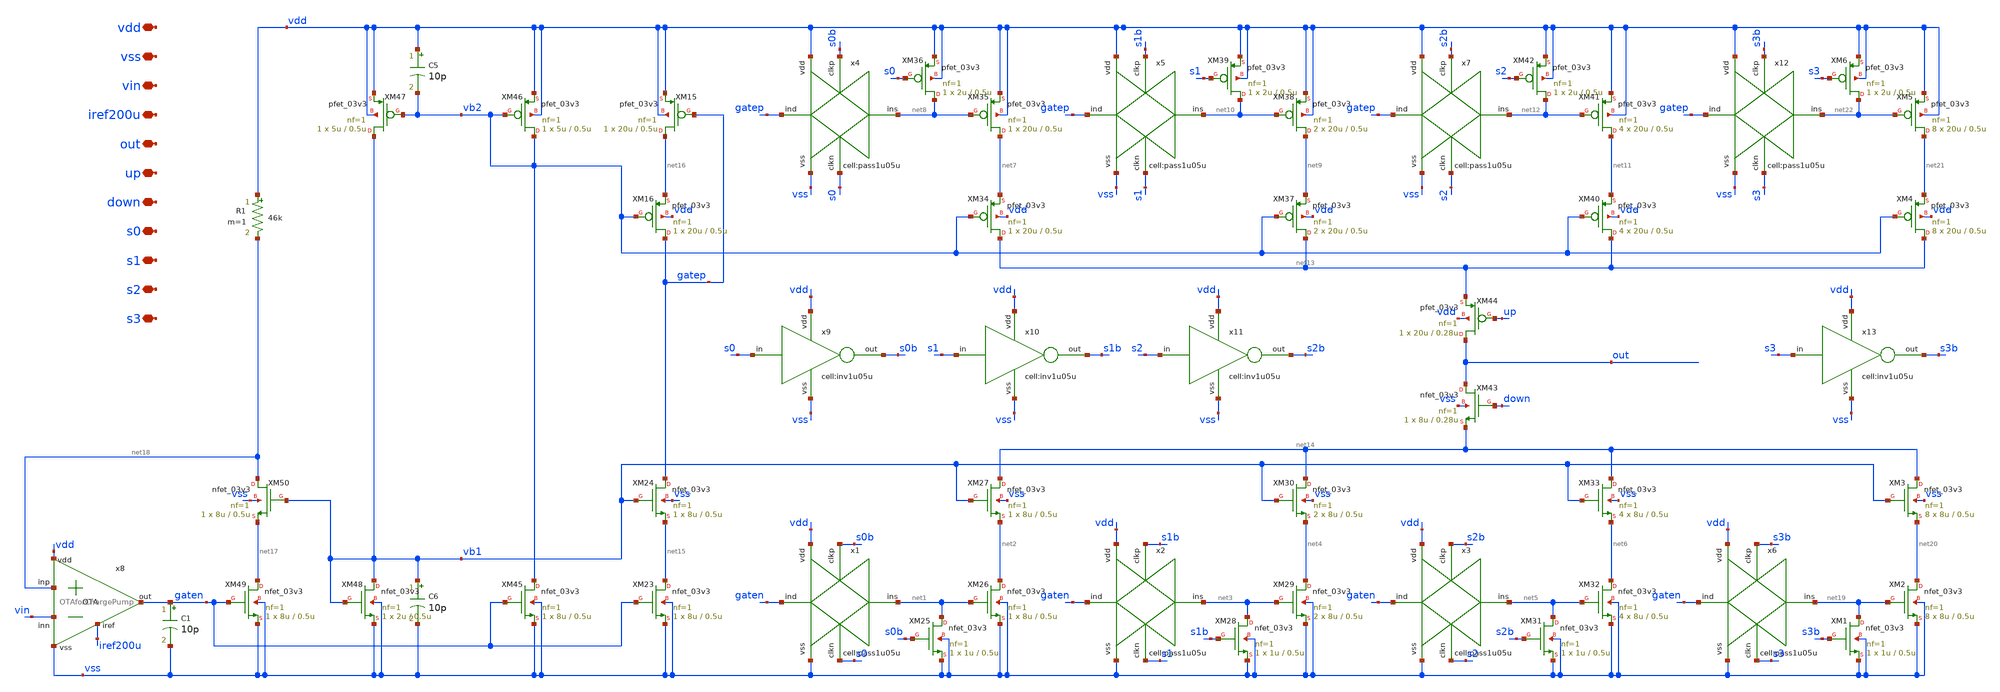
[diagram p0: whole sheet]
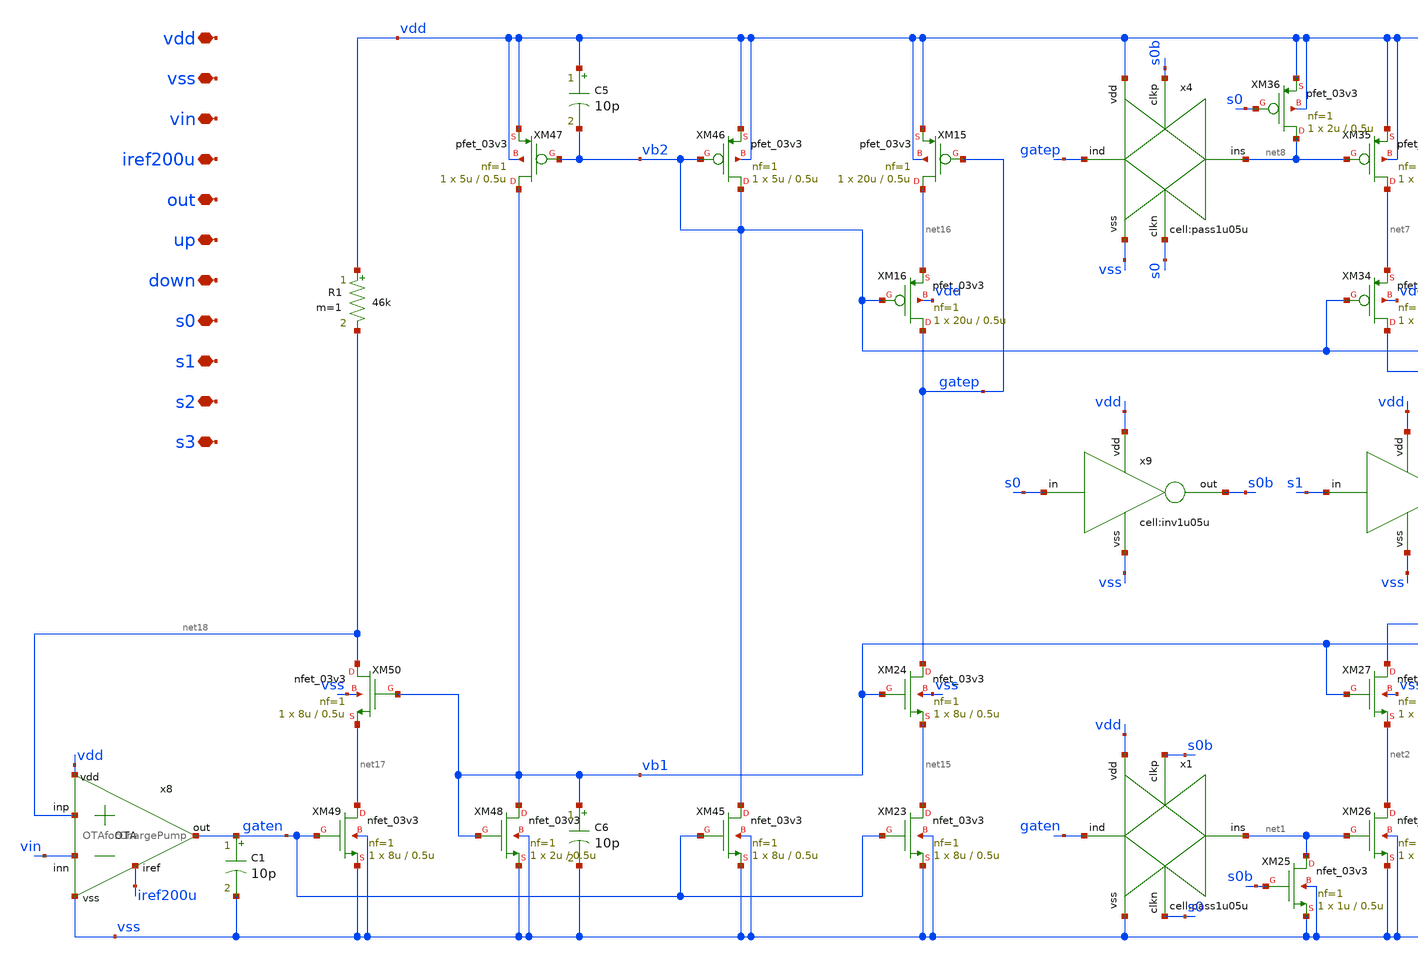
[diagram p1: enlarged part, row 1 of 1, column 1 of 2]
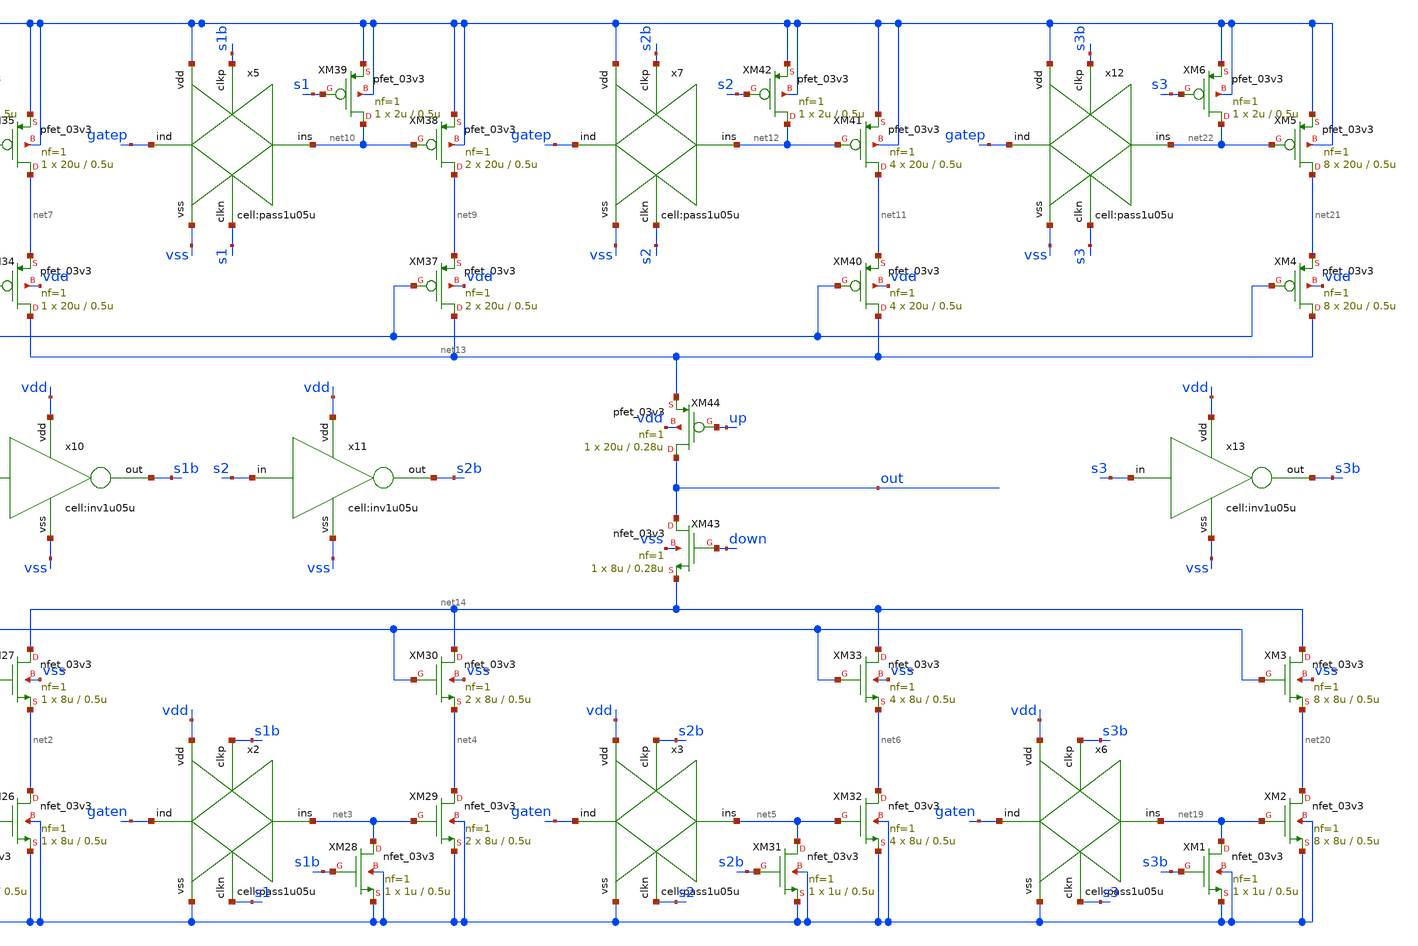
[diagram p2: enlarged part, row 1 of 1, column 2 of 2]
** sch_path: designs/libs/qw_core_analog/PCP1248X/PCP1248X.sch
**.subckt PCP1248X vdd vss vin iref200u out up down s0 s1 s2 s3
*.iopin vdd
*.iopin vss
*.iopin vin
*.iopin iref200u
*.iopin out
*.iopin up
*.iopin down
*.iopin s0
*.iopin s1
*.iopin s2
*.iopin s3
x1 gaten vss s0 net1 s0b vdd pass1u05u
XM25 net1 s0b vss vss nfet_03v3 L=0.5u W=1u nf=1 ad='int((nf+1)/2) * W/nf * 0.18u' as='int((nf+2)/2) * W/nf * 0.18u'
+ pd='2*int((nf+1)/2) * (W/nf + 0.18u)' ps='2*int((nf+2)/2) * (W/nf + 0.18u)' nrd='0.18u / W' nrs='0.18u / W'
+ sa=0 sb=0 sd=0 m=1
XM26 net2 net1 vss vss nfet_03v3 L=0.5u W=8u nf=1 ad='int((nf+1)/2) * W/nf * 0.18u' as='int((nf+2)/2) * W/nf * 0.18u'
+ pd='2*int((nf+1)/2) * (W/nf + 0.18u)' ps='2*int((nf+2)/2) * (W/nf + 0.18u)' nrd='0.18u / W' nrs='0.18u / W'
+ sa=0 sb=0 sd=0 m=1
XM27 net14 vb1 net2 vss nfet_03v3 L=0.5u W=8u nf=1 ad='int((nf+1)/2) * W/nf * 0.18u' as='int((nf+2)/2) * W/nf * 0.18u'
+ pd='2*int((nf+1)/2) * (W/nf + 0.18u)' ps='2*int((nf+2)/2) * (W/nf + 0.18u)' nrd='0.18u / W' nrs='0.18u / W'
+ sa=0 sb=0 sd=0 m=1
x2 gaten vss s1 net3 s1b vdd pass1u05u
XM28 net3 s1b vss vss nfet_03v3 L=0.5u W=1u nf=1 ad='int((nf+1)/2) * W/nf * 0.18u' as='int((nf+2)/2) * W/nf * 0.18u'
+ pd='2*int((nf+1)/2) * (W/nf + 0.18u)' ps='2*int((nf+2)/2) * (W/nf + 0.18u)' nrd='0.18u / W' nrs='0.18u / W'
+ sa=0 sb=0 sd=0 m=1
XM29 net4 net3 vss vss nfet_03v3 L=0.5u W=8u nf=1 ad='int((nf+1)/2) * W/nf * 0.18u' as='int((nf+2)/2) * W/nf * 0.18u'
+ pd='2*int((nf+1)/2) * (W/nf + 0.18u)' ps='2*int((nf+2)/2) * (W/nf + 0.18u)' nrd='0.18u / W' nrs='0.18u / W'
+ sa=0 sb=0 sd=0 m=2
XM30 net14 vb1 net4 vss nfet_03v3 L=0.5u W=8u nf=1 ad='int((nf+1)/2) * W/nf * 0.18u' as='int((nf+2)/2) * W/nf * 0.18u'
+ pd='2*int((nf+1)/2) * (W/nf + 0.18u)' ps='2*int((nf+2)/2) * (W/nf + 0.18u)' nrd='0.18u / W' nrs='0.18u / W'
+ sa=0 sb=0 sd=0 m=2
x3 gaten vss s2 net5 s2b vdd pass1u05u
XM31 net5 s2b vss vss nfet_03v3 L=0.5u W=1u nf=1 ad='int((nf+1)/2) * W/nf * 0.18u' as='int((nf+2)/2) * W/nf * 0.18u'
+ pd='2*int((nf+1)/2) * (W/nf + 0.18u)' ps='2*int((nf+2)/2) * (W/nf + 0.18u)' nrd='0.18u / W' nrs='0.18u / W'
+ sa=0 sb=0 sd=0 m=1
XM32 net6 net5 vss vss nfet_03v3 L=0.5u W=8u nf=1 ad='int((nf+1)/2) * W/nf * 0.18u' as='int((nf+2)/2) * W/nf * 0.18u'
+ pd='2*int((nf+1)/2) * (W/nf + 0.18u)' ps='2*int((nf+2)/2) * (W/nf + 0.18u)' nrd='0.18u / W' nrs='0.18u / W'
+ sa=0 sb=0 sd=0 m=4
XM33 net14 vb1 net6 vss nfet_03v3 L=0.5u W=8u nf=1 ad='int((nf+1)/2) * W/nf * 0.18u' as='int((nf+2)/2) * W/nf * 0.18u'
+ pd='2*int((nf+1)/2) * (W/nf + 0.18u)' ps='2*int((nf+2)/2) * (W/nf + 0.18u)' nrd='0.18u / W' nrs='0.18u / W'
+ sa=0 sb=0 sd=0 m=4
XM34 net13 vb2 net7 vdd pfet_03v3 L=0.5u W=20u nf=1 ad='int((nf+1)/2) * W/nf * 0.18u' as='int((nf+2)/2) * W/nf * 0.18u'
+ pd='2*int((nf+1)/2) * (W/nf + 0.18u)' ps='2*int((nf+2)/2) * (W/nf + 0.18u)' nrd='0.18u / W' nrs='0.18u / W'
+ sa=0 sb=0 sd=0 m=1
XM35 net7 net8 vdd vdd pfet_03v3 L=0.5u W=20u nf=1 ad='int((nf+1)/2) * W/nf * 0.18u' as='int((nf+2)/2) * W/nf * 0.18u'
+ pd='2*int((nf+1)/2) * (W/nf + 0.18u)' ps='2*int((nf+2)/2) * (W/nf + 0.18u)' nrd='0.18u / W' nrs='0.18u / W'
+ sa=0 sb=0 sd=0 m=1
x4 gatep vss s0 net8 s0b vdd pass1u05u
XM36 net8 s0 vdd vdd pfet_03v3 L=0.5u W=2u nf=1 ad='int((nf+1)/2) * W/nf * 0.18u' as='int((nf+2)/2) * W/nf * 0.18u'
+ pd='2*int((nf+1)/2) * (W/nf + 0.18u)' ps='2*int((nf+2)/2) * (W/nf + 0.18u)' nrd='0.18u / W' nrs='0.18u / W'
+ sa=0 sb=0 sd=0 m=1
XM37 net13 vb2 net9 vdd pfet_03v3 L=0.5u W=20u nf=1 ad='int((nf+1)/2) * W/nf * 0.18u' as='int((nf+2)/2) * W/nf * 0.18u'
+ pd='2*int((nf+1)/2) * (W/nf + 0.18u)' ps='2*int((nf+2)/2) * (W/nf + 0.18u)' nrd='0.18u / W' nrs='0.18u / W'
+ sa=0 sb=0 sd=0 m=2
XM38 net9 net10 vdd vdd pfet_03v3 L=0.5u W=20u nf=1 ad='int((nf+1)/2) * W/nf * 0.18u' as='int((nf+2)/2) * W/nf * 0.18u'
+ pd='2*int((nf+1)/2) * (W/nf + 0.18u)' ps='2*int((nf+2)/2) * (W/nf + 0.18u)' nrd='0.18u / W' nrs='0.18u / W'
+ sa=0 sb=0 sd=0 m=2
x5 gatep vss s1 net10 s1b vdd pass1u05u
XM39 net10 s1 vdd vdd pfet_03v3 L=0.5u W=2u nf=1 ad='int((nf+1)/2) * W/nf * 0.18u' as='int((nf+2)/2) * W/nf * 0.18u'
+ pd='2*int((nf+1)/2) * (W/nf + 0.18u)' ps='2*int((nf+2)/2) * (W/nf + 0.18u)' nrd='0.18u / W' nrs='0.18u / W'
+ sa=0 sb=0 sd=0 m=1
XM40 net13 vb2 net11 vdd pfet_03v3 L=0.5u W=20u nf=1 ad='int((nf+1)/2) * W/nf * 0.18u' as='int((nf+2)/2) * W/nf * 0.18u'
+ pd='2*int((nf+1)/2) * (W/nf + 0.18u)' ps='2*int((nf+2)/2) * (W/nf + 0.18u)' nrd='0.18u / W' nrs='0.18u / W'
+ sa=0 sb=0 sd=0 m=4
XM41 net11 net12 vdd vdd pfet_03v3 L=0.5u W=20u nf=1 ad='int((nf+1)/2) * W/nf * 0.18u' as='int((nf+2)/2) * W/nf * 0.18u'
+ pd='2*int((nf+1)/2) * (W/nf + 0.18u)' ps='2*int((nf+2)/2) * (W/nf + 0.18u)' nrd='0.18u / W' nrs='0.18u / W'
+ sa=0 sb=0 sd=0 m=4
x7 gatep vss s2 net12 s2b vdd pass1u05u
XM42 net12 s2 vdd vdd pfet_03v3 L=0.5u W=2u nf=1 ad='int((nf+1)/2) * W/nf * 0.18u' as='int((nf+2)/2) * W/nf * 0.18u'
+ pd='2*int((nf+1)/2) * (W/nf + 0.18u)' ps='2*int((nf+2)/2) * (W/nf + 0.18u)' nrd='0.18u / W' nrs='0.18u / W'
+ sa=0 sb=0 sd=0 m=1
XM43 out down net14 vss nfet_03v3 L=0.28u W=8u nf=1 ad='int((nf+1)/2) * W/nf * 0.18u' as='int((nf+2)/2) * W/nf * 0.18u'
+ pd='2*int((nf+1)/2) * (W/nf + 0.18u)' ps='2*int((nf+2)/2) * (W/nf + 0.18u)' nrd='0.18u / W' nrs='0.18u / W'
+ sa=0 sb=0 sd=0 m=1
XM44 out up net13 vdd pfet_03v3 L=0.28u W=20u nf=1 ad='int((nf+1)/2) * W/nf * 0.18u' as='int((nf+2)/2) * W/nf * 0.18u'
+ pd='2*int((nf+1)/2) * (W/nf + 0.18u)' ps='2*int((nf+2)/2) * (W/nf + 0.18u)' nrd='0.18u / W' nrs='0.18u / W'
+ sa=0 sb=0 sd=0 m=1
XM15 net16 gatep vdd vdd pfet_03v3 L=0.5u W=20u nf=1 ad='int((nf+1)/2) * W/nf * 0.18u' as='int((nf+2)/2) * W/nf * 0.18u'
+ pd='2*int((nf+1)/2) * (W/nf + 0.18u)' ps='2*int((nf+2)/2) * (W/nf + 0.18u)' nrd='0.18u / W' nrs='0.18u / W'
+ sa=0 sb=0 sd=0 m=1
XM16 gatep vb2 net16 vdd pfet_03v3 L=0.5u W=20u nf=1 ad='int((nf+1)/2) * W/nf * 0.18u' as='int((nf+2)/2) * W/nf * 0.18u'
+ pd='2*int((nf+1)/2) * (W/nf + 0.18u)' ps='2*int((nf+2)/2) * (W/nf + 0.18u)' nrd='0.18u / W' nrs='0.18u / W'
+ sa=0 sb=0 sd=0 m=1
XM23 net15 gaten vss vss nfet_03v3 L=0.5u W=8u nf=1 ad='int((nf+1)/2) * W/nf * 0.18u' as='int((nf+2)/2) * W/nf * 0.18u'
+ pd='2*int((nf+1)/2) * (W/nf + 0.18u)' ps='2*int((nf+2)/2) * (W/nf + 0.18u)' nrd='0.18u / W' nrs='0.18u / W'
+ sa=0 sb=0 sd=0 m=1
XM24 gatep vb1 net15 vss nfet_03v3 L=0.5u W=8u nf=1 ad='int((nf+1)/2) * W/nf * 0.18u' as='int((nf+2)/2) * W/nf * 0.18u'
+ pd='2*int((nf+1)/2) * (W/nf + 0.18u)' ps='2*int((nf+2)/2) * (W/nf + 0.18u)' nrd='0.18u / W' nrs='0.18u / W'
+ sa=0 sb=0 sd=0 m=1
XM45 vb2 gaten vss vss nfet_03v3 L=0.5u W=8u nf=1 ad='int((nf+1)/2) * W/nf * 0.18u' as='int((nf+2)/2) * W/nf * 0.18u'
+ pd='2*int((nf+1)/2) * (W/nf + 0.18u)' ps='2*int((nf+2)/2) * (W/nf + 0.18u)' nrd='0.18u / W' nrs='0.18u / W'
+ sa=0 sb=0 sd=0 m=1
XM46 vb2 vb2 vdd vdd pfet_03v3 L=0.5u W=5u nf=1 ad='int((nf+1)/2) * W/nf * 0.18u' as='int((nf+2)/2) * W/nf * 0.18u'
+ pd='2*int((nf+1)/2) * (W/nf + 0.18u)' ps='2*int((nf+2)/2) * (W/nf + 0.18u)' nrd='0.18u / W' nrs='0.18u / W'
+ sa=0 sb=0 sd=0 m=1
XM47 vb1 vb2 vdd vdd pfet_03v3 L=0.5u W=5u nf=1 ad='int((nf+1)/2) * W/nf * 0.18u' as='int((nf+2)/2) * W/nf * 0.18u'
+ pd='2*int((nf+1)/2) * (W/nf + 0.18u)' ps='2*int((nf+2)/2) * (W/nf + 0.18u)' nrd='0.18u / W' nrs='0.18u / W'
+ sa=0 sb=0 sd=0 m=1
XM48 vb1 vb1 vss vss nfet_03v3 L=0.5u W=2u nf=1 ad='int((nf+1)/2) * W/nf * 0.18u' as='int((nf+2)/2) * W/nf * 0.18u'
+ pd='2*int((nf+1)/2) * (W/nf + 0.18u)' ps='2*int((nf+2)/2) * (W/nf + 0.18u)' nrd='0.18u / W' nrs='0.18u / W'
+ sa=0 sb=0 sd=0 m=1
XM49 net17 gaten vss vss nfet_03v3 L=0.5u W=8u nf=1 ad='int((nf+1)/2) * W/nf * 0.18u' as='int((nf+2)/2) * W/nf * 0.18u'
+ pd='2*int((nf+1)/2) * (W/nf + 0.18u)' ps='2*int((nf+2)/2) * (W/nf + 0.18u)' nrd='0.18u / W' nrs='0.18u / W'
+ sa=0 sb=0 sd=0 m=1
XM50 net18 vb1 net17 vss nfet_03v3 L=0.5u W=8u nf=1 ad='int((nf+1)/2) * W/nf * 0.18u' as='int((nf+2)/2) * W/nf * 0.18u'
+ pd='2*int((nf+1)/2) * (W/nf + 0.18u)' ps='2*int((nf+2)/2) * (W/nf + 0.18u)' nrd='0.18u / W' nrs='0.18u / W'
+ sa=0 sb=0 sd=0 m=1
x8 vdd iref200u net18 vin gaten vss OTAforChargePump
R1 vdd net18 46k m=1
C1 gaten vss 10p m=1
C5 vdd vb2 10p m=1
x9 s0 vdd s0b vss inv1u05u
C6 vb1 vss 10p m=1
x10 s1 vdd s1b vss inv1u05u
x11 s2 vdd s2b vss inv1u05u
x6 gaten vss s3 net19 s3b vdd pass1u05u
XM1 net19 s3b vss vss nfet_03v3 L=0.5u W=1u nf=1 ad='int((nf+1)/2) * W/nf * 0.18u' as='int((nf+2)/2) * W/nf * 0.18u'
+ pd='2*int((nf+1)/2) * (W/nf + 0.18u)' ps='2*int((nf+2)/2) * (W/nf + 0.18u)' nrd='0.18u / W' nrs='0.18u / W'
+ sa=0 sb=0 sd=0 m=1
XM2 net20 net19 vss vss nfet_03v3 L=0.5u W=8u nf=1 ad='int((nf+1)/2) * W/nf * 0.18u' as='int((nf+2)/2) * W/nf * 0.18u'
+ pd='2*int((nf+1)/2) * (W/nf + 0.18u)' ps='2*int((nf+2)/2) * (W/nf + 0.18u)' nrd='0.18u / W' nrs='0.18u / W'
+ sa=0 sb=0 sd=0 m=8
XM3 net14 vb1 net20 vss nfet_03v3 L=0.5u W=8u nf=1 ad='int((nf+1)/2) * W/nf * 0.18u' as='int((nf+2)/2) * W/nf * 0.18u'
+ pd='2*int((nf+1)/2) * (W/nf + 0.18u)' ps='2*int((nf+2)/2) * (W/nf + 0.18u)' nrd='0.18u / W' nrs='0.18u / W'
+ sa=0 sb=0 sd=0 m=8
XM4 net13 vb2 net21 vdd pfet_03v3 L=0.5u W=20u nf=1 ad='int((nf+1)/2) * W/nf * 0.18u' as='int((nf+2)/2) * W/nf * 0.18u'
+ pd='2*int((nf+1)/2) * (W/nf + 0.18u)' ps='2*int((nf+2)/2) * (W/nf + 0.18u)' nrd='0.18u / W' nrs='0.18u / W'
+ sa=0 sb=0 sd=0 m=8
XM5 net21 net22 vdd vdd pfet_03v3 L=0.5u W=20u nf=1 ad='int((nf+1)/2) * W/nf * 0.18u' as='int((nf+2)/2) * W/nf * 0.18u'
+ pd='2*int((nf+1)/2) * (W/nf + 0.18u)' ps='2*int((nf+2)/2) * (W/nf + 0.18u)' nrd='0.18u / W' nrs='0.18u / W'
+ sa=0 sb=0 sd=0 m=8
x12 gatep vss s3 net22 s3b vdd pass1u05u
XM6 net22 s3 vdd vdd pfet_03v3 L=0.5u W=2u nf=1 ad='int((nf+1)/2) * W/nf * 0.18u' as='int((nf+2)/2) * W/nf * 0.18u'
+ pd='2*int((nf+1)/2) * (W/nf + 0.18u)' ps='2*int((nf+2)/2) * (W/nf + 0.18u)' nrd='0.18u / W' nrs='0.18u / W'
+ sa=0 sb=0 sd=0 m=1
x13 s3 vdd s3b vss inv1u05u
**.ends
.end
